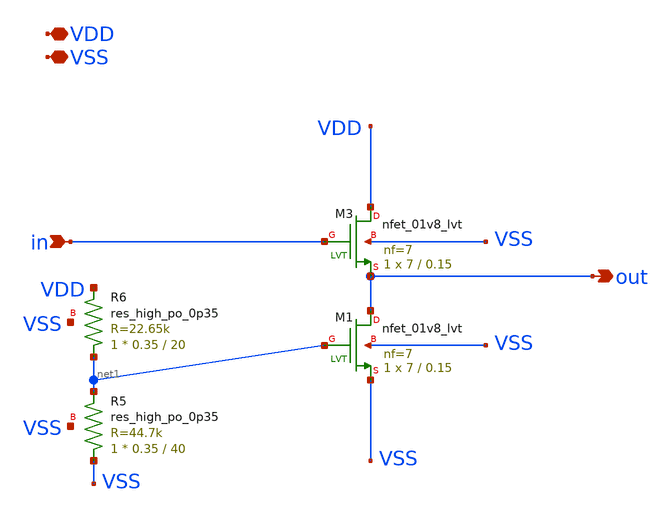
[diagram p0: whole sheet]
** sch_path: xschem/buffer.sch
**.subckt buffer VSS VDD in out
*.iopin VSS
*.iopin VDD
*.ipin in
*.opin out
XM3 VDD in out VSS sky130_fd_pr__nfet_01v8_lvt L=0.15 W=7 nf=7 ad='int((nf+1)/2) * W/nf * 0.29' as='int((nf+2)/2) * W/nf * 0.29'
+ pd='2*int((nf+1)/2) * (W/nf + 0.29)' ps='2*int((nf+2)/2) * (W/nf + 0.29)' nrd='0.29 / W' nrs='0.29 / W'
+ sa=0 sb=0 sd=0 mult=1 m=1
XM1 out net1 VSS VSS sky130_fd_pr__nfet_01v8_lvt L=0.15 W=7 nf=7 ad='int((nf+1)/2) * W/nf * 0.29' as='int((nf+2)/2) * W/nf * 0.29'
+ pd='2*int((nf+1)/2) * (W/nf + 0.29)' ps='2*int((nf+2)/2) * (W/nf + 0.29)' nrd='0.29 / W' nrs='0.29 / W'
+ sa=0 sb=0 sd=0 mult=1 m=1
XR5 VSS net1 VSS sky130_fd_pr__res_high_po_0p35 L=40 mult=1 m=1
XR6 net1 VDD VSS sky130_fd_pr__res_high_po_0p35 L=20 mult=1 m=1
**.ends
.end
